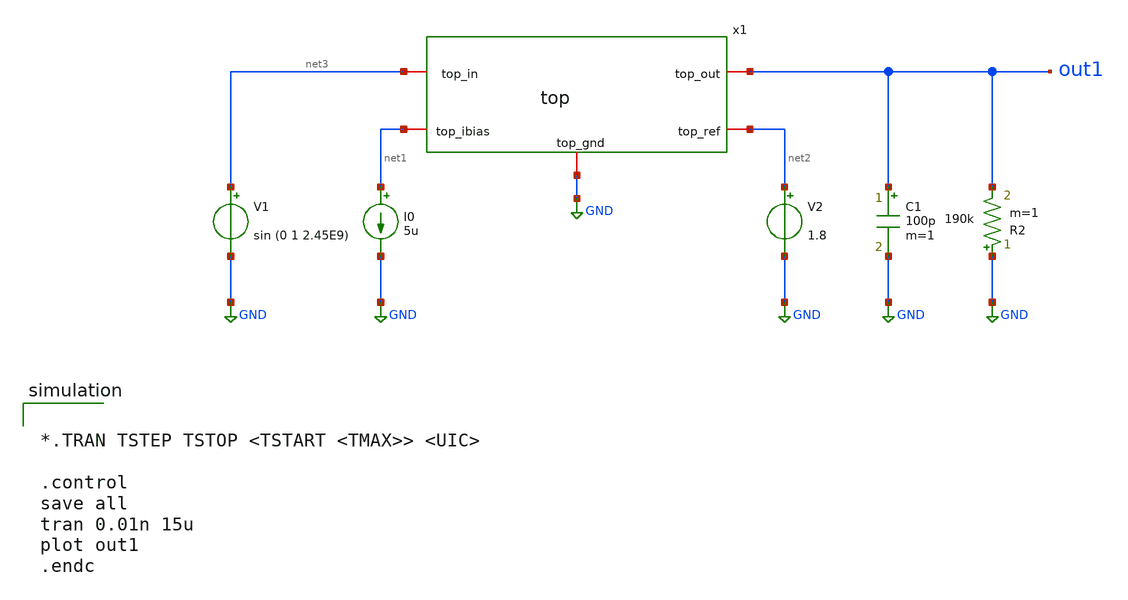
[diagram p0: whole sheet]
** sch_path: xschem/tb-top.sch
**.subckt tb-top
V1 net3 GND sin (0 1 2.45E9)
R2 GND out1 190k m=1
I0 net1 GND 5u
V2 net2 GND 1.8
C1 out1 GND 100p m=1
x1 net3 out1 net2 net1 GND top
**** begin user architecture code


*.TRAN TSTEP TSTOP <TSTART <TMAX>> <UIC>

.control
save all
tran 0.01n 15u
plot out1
.endc



** opencircuitdesign pdks install
.lib $::SKYWATER_MODELS/sky130.lib.spice tt


**** end user architecture code
**.ends
.GLOBAL GND
.end
